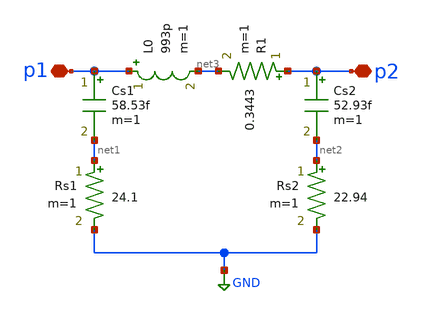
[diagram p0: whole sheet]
** sch_path: xschem-2.45GHz/l1-2.45G.sch
**.subckt l1-2.45G p2 p1
*.iopin p2
*.iopin p1
L0 p1 net3 993p m=1
Cs1 p1 net1 58.53f m=1
Cs2 p2 net2 52.93f m=1
Rs1 net1 GND 24.1 m=1
Rs2 net2 GND 22.94 m=1
R1 p2 net3 0.3443 m=1
**.ends
.GLOBAL GND
.end
